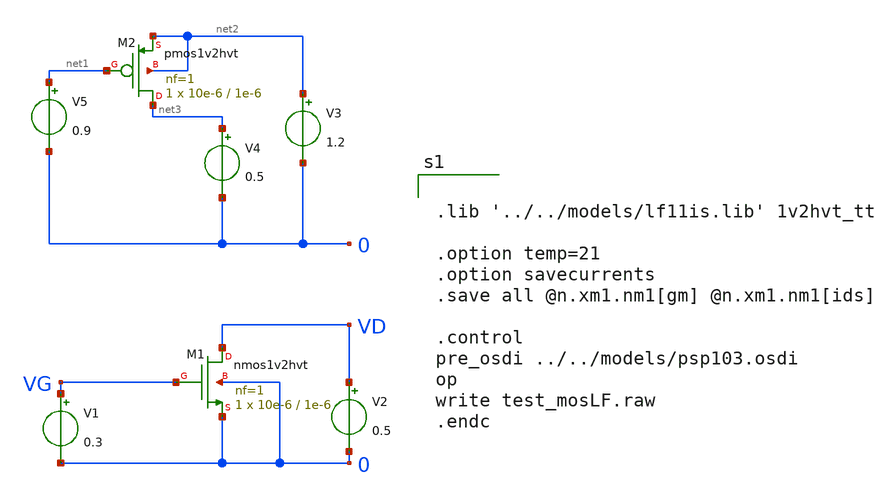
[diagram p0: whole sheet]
** sch_path: test_mosLF.sch
**.subckt test_mosLF
V1 VG 0 0.3
V2 VD 0 0.5
XM1 VD VG 0 0 nmos1v2hvt L=1e-6 W=10e-6 nf=1 abdrain='int((nf+1)/2) * W/nf * 0.29' absource='int((nf+2)/2) * W/nf * 0.29'
+ lsdrain='2*int((nf+1)/2) * (W/nf + 0.29)' lssource='2*int((nf+2)/2) * (W/nf + 0.29)' dta=0 nrd='0.29 / W'
+ nrs='0.29 / W' sa=0 sb=0 sd=0 mult=1 m=1
V3 net2 0 1.2
V4 net3 0 0.5
V5 net1 0 0.9
XM2 net3 net1 net2 net2 pmos1v2hvt L=1e-6 W=10e-6 nf=1 abdrain='int((nf+1)/2) * W/nf * 0.29' absource='int((nf+2)/2) * W/nf * 0.29'
+ lsdrain='2*int((nf+1)/2) * (W/nf + 0.29)' lssource='2*int((nf+2)/2) * (W/nf + 0.29)' dta=0 nrd='0.29 / W'
+ nrs='0.29 / W' sa=0 sb=0 sd=0 mult=1 m=1
**** begin user architecture code


.lib '../../models/lf11is.lib' 1v2hvt_tt

.option temp=21
.option savecurrents
.save all @n.xm1.nm1[gm] @n.xm1.nm1[ids]

.control
pre_osdi ../../models/psp103.osdi
op
write test_mosLF.raw
.endc


**** end user architecture code
**.ends
.end
